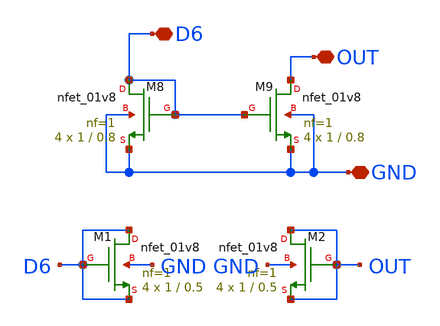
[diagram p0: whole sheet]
** sch_path: block4/xschem/block4.sch
**.subckt block4 GND D6 OUT
*.iopin GND
*.iopin D6
*.iopin OUT
XM8 D6 D6 GND GND sky130_fd_pr__nfet_01v8 L=0.8 W=1 nf=1 ad='int((nf+1)/2) * W/nf * 0.29' as='int((nf+2)/2) * W/nf * 0.29'
+ pd='2*int((nf+1)/2) * (W/nf + 0.29)' ps='2*int((nf+2)/2) * (W/nf + 0.29)' nrd='0.29 / W' nrs='0.29 / W'
+ sa=0 sb=0 sd=0 mult=4 m=4
XM9 OUT D6 GND GND sky130_fd_pr__nfet_01v8 L=0.8 W=1 nf=1 ad='int((nf+1)/2) * W/nf * 0.29' as='int((nf+2)/2) * W/nf * 0.29'
+ pd='2*int((nf+1)/2) * (W/nf + 0.29)' ps='2*int((nf+2)/2) * (W/nf + 0.29)' nrd='0.29 / W' nrs='0.29 / W'
+ sa=0 sb=0 sd=0 mult=4 m=4
XM1 D6 D6 D6 GND sky130_fd_pr__nfet_01v8 L=0.5 W=1 nf=1 ad='int((nf+1)/2) * W/nf * 0.29' as='int((nf+2)/2) * W/nf * 0.29'
+ pd='2*int((nf+1)/2) * (W/nf + 0.29)' ps='2*int((nf+2)/2) * (W/nf + 0.29)' nrd='0.29 / W' nrs='0.29 / W'
+ sa=0 sb=0 sd=0 mult=4 m=4
XM2 OUT OUT OUT GND sky130_fd_pr__nfet_01v8 L=0.5 W=1 nf=1 ad='int((nf+1)/2) * W/nf * 0.29' as='int((nf+2)/2) * W/nf * 0.29'
+ pd='2*int((nf+1)/2) * (W/nf + 0.29)' ps='2*int((nf+2)/2) * (W/nf + 0.29)' nrd='0.29 / W' nrs='0.29 / W'
+ sa=0 sb=0 sd=0 mult=4 m=4
**.ends
.end
